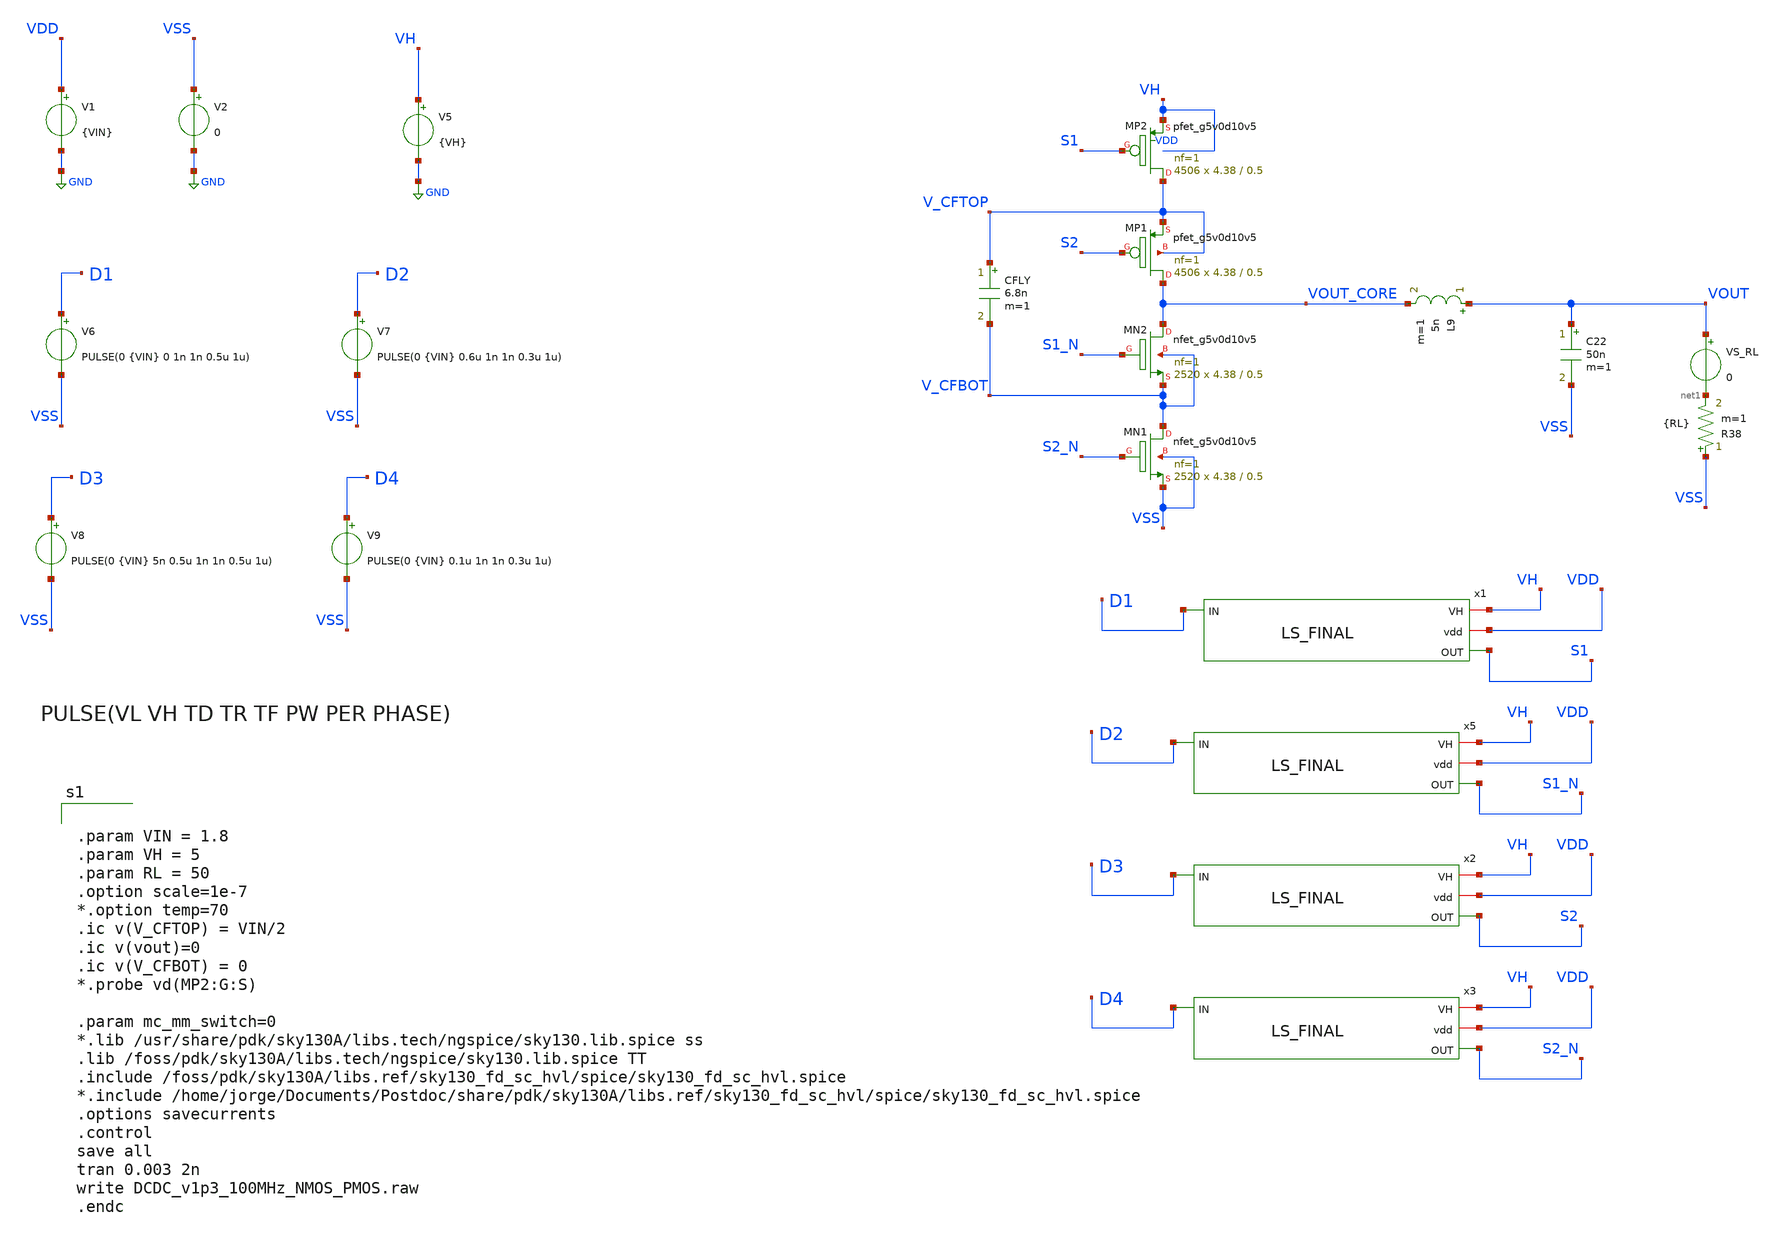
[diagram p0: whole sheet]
** sch_path: xschem/dev_switches/DCDC_5V_FINAL/DCDC_v1p3_100MHz_NMOS_PMOS_jm.sch
* Copyright 2021 Stefan Frederik Schippers
**.subckt DCDC_v1p3_100MHz_NMOS_PMOS_jm
XMN2 VOUT_CORE S1_N V_CFBOT V_CFBOT sky130_fd_pr__nfet_g5v0d10v5 L=0.5 W=4.38 nf=1 ad='int((nf+1)/2) * W/nf * 0.29'
+ as='int((nf+2)/2) * W/nf * 0.29' pd='2*int((nf+1)/2) * (W/nf + 0.29)' ps='2*int((nf+2)/2) * (W/nf + 0.29)'
+ nrd='0.29 / W' nrs='0.29 / W' sa=0 sb=0 sd=0 mult=2520 m=2520
XMN1 V_CFBOT S2_N VSS VSS sky130_fd_pr__nfet_g5v0d10v5 L=0.5 W=4.38 nf=1 ad='int((nf+1)/2) * W/nf * 0.29'
+ as='int((nf+2)/2) * W/nf * 0.29' pd='2*int((nf+1)/2) * (W/nf + 0.29)' ps='2*int((nf+2)/2) * (W/nf + 0.29)'
+ nrd='0.29 / W' nrs='0.29 / W' sa=0 sb=0 sd=0 mult=2520 m=2520
CFLY V_CFTOP V_CFBOT 6.8n m=1
L9 VOUT VOUT_CORE 5n m=1
C22 VOUT VSS 50n m=1
R38 VSS net1 {RL} m=1
VS_RL VOUT net1 0
XMP2 V_CFTOP S1 VH VDD sky130_fd_pr__pfet_g5v0d10v5 L=0.5 W=4.38 nf=1 ad='int((nf+1)/2) * W/nf * 0.29'
+ as='int((nf+2)/2) * W/nf * 0.29' pd='2*int((nf+1)/2) * (W/nf + 0.29)' ps='2*int((nf+2)/2) * (W/nf + 0.29)'
+ nrd='0.29 / W' nrs='0.29 / W' sa=0 sb=0 sd=0 mult=4506 m=4506
XMP1 VOUT_CORE S2 V_CFTOP V_CFTOP sky130_fd_pr__pfet_g5v0d10v5 L=0.5 W=4.38 nf=1 ad='int((nf+1)/2) * W/nf * 0.29'
+ as='int((nf+2)/2) * W/nf * 0.29' pd='2*int((nf+1)/2) * (W/nf + 0.29)' ps='2*int((nf+2)/2) * (W/nf + 0.29)'
+ nrd='0.29 / W' nrs='0.29 / W' sa=0 sb=0 sd=0 mult=4506 m=4506
x1 VH VDD S1 D1 LS_FINAL
x2 VH VDD S2 D3 LS_FINAL
x3 VH VDD S2_N D4 LS_FINAL
x5 VH VDD S1_N D2 LS_FINAL
V6 D1 VSS PULSE(0 {VIN} 0 1n 1n 0.5u 1u)
V7 D2 VSS PULSE(0 {VIN} 0.6u 1n 1n 0.3u 1u)
V1 VDD GND {VIN}
V2 VSS GND 0
V5 VH GND {VH}
V8 D3 VSS PULSE(0 {VIN} 5n 0.5u 1n 1n 0.5u 1u)
V9 D4 VSS PULSE(0 {VIN} 0.1u 1n 1n 0.3u 1u)
**** begin user architecture code


.param VIN = 1.8
.param VH = 5
.param RL = 50
.option scale=1e-7
*.option temp=70
.ic v(V_CFTOP) = VIN/2
.ic v(vout)=0
.ic v(V_CFBOT) = 0
*.probe vd(MP2:G:S)

.param mc_mm_switch=0
*.lib /usr/share/pdk/sky130A/libs.tech/ngspice/sky130.lib.spice ss
.lib /foss/pdk/sky130A/libs.tech/ngspice/sky130.lib.spice TT
.include /foss/pdk/sky130A/libs.ref/sky130_fd_sc_hvl/spice/sky130_fd_sc_hvl.spice
*.include /home/jorge/Documents/Postdoc/share/pdk/sky130A/libs.ref/sky130_fd_sc_hvl/spice/sky130_fd_sc_hvl.spice
.options savecurrents
.control
save all
tran 0.003 2n
write DCDC_v1p3_100MHz_NMOS_PMOS.raw
.endc


**** end user architecture code
**.ends

* expanding   symbol:  LS_FINAL.sym # of pins=4
** sym_path: xschem/dev_switches/DCDC_5V_FINAL/LS_FINAL.sym
** sch_path: xschem/dev_switches/DCDC_5V_FINAL/LS_FINAL.sch
.subckt LS_FINAL VH vdd OUT IN
*.ipin IN
*.iopin vdd
*.iopin VH
*.opin OUT
XM11 net1 IN vdd vdd sky130_fd_pr__pfet_01v8 L=0.15 W=5 nf=1 ad='int((nf+1)/2) * W/nf * 0.29' as='int((nf+2)/2) * W/nf * 0.29'
+ pd='2*int((nf+1)/2) * (W/nf + 0.29)' ps='2*int((nf+2)/2) * (W/nf + 0.29)' nrd='0.29 / W' nrs='0.29 / W'
+ sa=0 sb=0 sd=0 mult=1 m=1
XM12 net1 IN GND GND sky130_fd_pr__nfet_01v8 L=0.15 W=5 nf=1 ad='int((nf+1)/2) * W/nf * 0.29' as='int((nf+2)/2) * W/nf * 0.29'
+ pd='2*int((nf+1)/2) * (W/nf + 0.29)' ps='2*int((nf+2)/2) * (W/nf + 0.29)' nrd='0.29 / W' nrs='0.29 / W'
+ sa=0 sb=0 sd=0 mult=1 m=1
XM15 net2 net3 VH VH sky130_fd_pr__pfet_g5v0d10v5 L=0.5 W=2 nf=1 ad='int((nf+1)/2) * W/nf * 0.29' as='int((nf+2)/2) * W/nf * 0.29'
+ pd='2*int((nf+1)/2) * (W/nf + 0.29)' ps='2*int((nf+2)/2) * (W/nf + 0.29)' nrd='0.29 / W' nrs='0.29 / W'
+ sa=0 sb=0 sd=0 mult=1 m=1
XM14 net3 net2 VH VH sky130_fd_pr__pfet_g5v0d10v5 L=0.5 W=2 nf=1 ad='int((nf+1)/2) * W/nf * 0.29' as='int((nf+2)/2) * W/nf * 0.29'
+ pd='2*int((nf+1)/2) * (W/nf + 0.29)' ps='2*int((nf+2)/2) * (W/nf + 0.29)' nrd='0.29 / W' nrs='0.29 / W'
+ sa=0 sb=0 sd=0 mult=1 m=1
XM16 net4 net2 VH VH sky130_fd_pr__pfet_g5v0d10v5 L=0.5 W=10 nf=1 ad='int((nf+1)/2) * W/nf * 0.29' as='int((nf+2)/2) * W/nf * 0.29'
+ pd='2*int((nf+1)/2) * (W/nf + 0.29)' ps='2*int((nf+2)/2) * (W/nf + 0.29)' nrd='0.29 / W' nrs='0.29 / W'
+ sa=0 sb=0 sd=0 mult=10 m=10
XM18 net2 net1 GND GND sky130_fd_pr__nfet_g5v0d10v5 L=0.5 W=12 nf=1 ad='int((nf+1)/2) * W/nf * 0.29'
+ as='int((nf+2)/2) * W/nf * 0.29' pd='2*int((nf+1)/2) * (W/nf + 0.29)' ps='2*int((nf+2)/2) * (W/nf + 0.29)'
+ nrd='0.29 / W' nrs='0.29 / W' sa=0 sb=0 sd=0 mult=1 m=1
XM13 net3 IN GND GND sky130_fd_pr__nfet_g5v0d10v5 L=0.5 W=12 nf=1 ad='int((nf+1)/2) * W/nf * 0.29' as='int((nf+2)/2) * W/nf * 0.29'
+ pd='2*int((nf+1)/2) * (W/nf + 0.29)' ps='2*int((nf+2)/2) * (W/nf + 0.29)' nrd='0.29 / W' nrs='0.29 / W'
+ sa=0 sb=0 sd=0 mult=1 m=1
XM17 net4 IN GND GND sky130_fd_pr__nfet_g5v0d10v5 L=0.5 W=10 nf=1 ad='int((nf+1)/2) * W/nf * 0.29' as='int((nf+2)/2) * W/nf * 0.29'
+ pd='2*int((nf+1)/2) * (W/nf + 0.29)' ps='2*int((nf+2)/2) * (W/nf + 0.29)' nrd='0.29 / W' nrs='0.29 / W'
+ sa=0 sb=0 sd=0 mult=10 m=10
XM7 OUT net4 VH VH sky130_fd_pr__pfet_g5v0d10v5 L=0.5 W=10 nf=1 ad='int((nf+1)/2) * W/nf * 0.29' as='int((nf+2)/2) * W/nf * 0.29'
+ pd='2*int((nf+1)/2) * (W/nf + 0.29)' ps='2*int((nf+2)/2) * (W/nf + 0.29)' nrd='0.29 / W' nrs='0.29 / W'
+ sa=0 sb=0 sd=0 mult={multip} m={multip}
XM10 OUT net4 GND GND sky130_fd_pr__nfet_g5v0d10v5 L=0.5 W=10 nf=1 ad='int((nf+1)/2) * W/nf * 0.29' as='int((nf+2)/2) * W/nf * 0.29'
+ pd='2*int((nf+1)/2) * (W/nf + 0.29)' ps='2*int((nf+2)/2) * (W/nf + 0.29)' nrd='0.29 / W' nrs='0.29 / W'
+ sa=0 sb=0 sd=0 mult={multip} m={multip}
**** begin user architecture code

*
* Parameters

*.PARAM BAT=1.8
.PARAM W12=12 W45=2 LLS=0.5 multip=40
*.option scale=1e-6
*.options TEMP = 65.0

* Models
*.lib /foss/pdk/sky130A/libs.tech/ngspice/sky130.lib.spice TT

*Fuentes******
*VBAT VDD 0 DC BAT
*VHIGH VH 0 DC 5
*vin IN 0 dc 0 PULSE (0 BAT .1n .1n .1n 10n 20n)

*COUT OUT 0 20p


*.options savecurrents
*.save all
*+ @M.XM12.msky130_fd_pr_nfet_01v8[id]

*.control
*tran 0.1n 100n
*plot v(IN) v(LS1) v(OUT) v(net6) i(@M.XM12.msky130_fd_pr_nfet_01v8[id])
*write LS_FINAL.raw
*.endc
*.end
*

**** end user architecture code
.ends

.GLOBAL GND
.end
